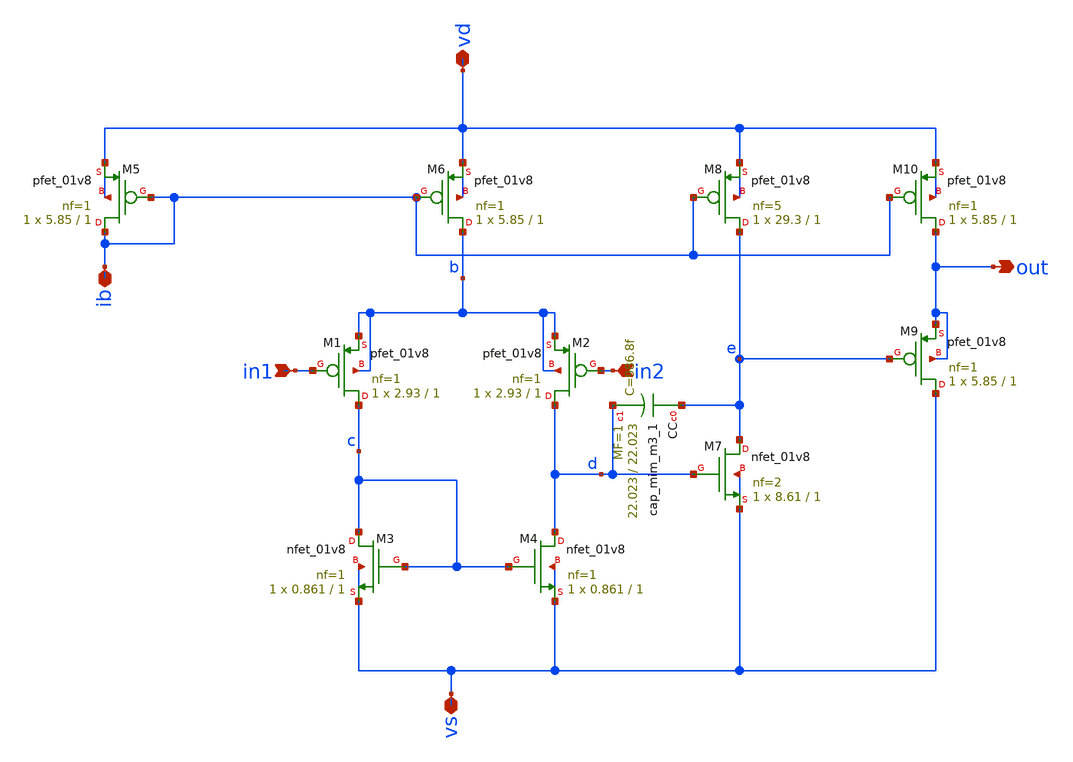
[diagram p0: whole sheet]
** sch_path: xschem/ota.sch
* Copyright 2020 Stefan Frederik Schippers
* Licensed under the Apache License, Version 2.0 (the "License");
* you may not use this file except in compliance with the License.
* You may obtain a copy of the License at
* https://www.apache.org/licenses/LICENSE-2.0
* Unless required by applicable law or agreed to in writing, software
* distributed under the License is distributed on an "AS IS" BASIS,
* WITHOUT WARRANTIES OR CONDITIONS OF ANY KIND, either express or implied.
* See the License for the specific language governing permissions and
* limitations under the License.
**.subckt ota vd vs ib in1 in2 out
*.iopin vd
*.iopin vs
*.iopin ib
*.ipin in1
*.ipin in2
*.opin out
XM4 d c vs vs sky130_fd_pr__nfet_01v8 L=1 W=0.861 nf=1 ad='int((nf+1)/2) * W/nf * 0.29' as='int((nf+2)/2) * W/nf * 0.29'
+ pd='2*int((nf+1)/2) * (W/nf + 0.29)' ps='2*int((nf+2)/2) * (W/nf + 0.29)' nrd='0.29 / W' nrs='0.29 / W'
+ sa=0 sb=0 sd=0 mult=1 m=1
XM7 e d vs vs sky130_fd_pr__nfet_01v8 L=1 W=8.61 nf=2 ad='int((nf+1)/2) * W/nf * 0.29' as='int((nf+2)/2) * W/nf * 0.29'
+ pd='2*int((nf+1)/2) * (W/nf + 0.29)' ps='2*int((nf+2)/2) * (W/nf + 0.29)' nrd='0.29 / W' nrs='0.29 / W'
+ sa=0 sb=0 sd=0 mult=1 m=1
XM5 ib ib vd vd sky130_fd_pr__pfet_01v8 L=1 W=5.85 nf=1 ad='int((nf+1)/2) * W/nf * 0.29' as='int((nf+2)/2) * W/nf * 0.29'
+ pd='2*int((nf+1)/2) * (W/nf + 0.29)' ps='2*int((nf+2)/2) * (W/nf + 0.29)' nrd='0.29 / W' nrs='0.29 / W'
+ sa=0 sb=0 sd=0 mult=1 m=1
XM6 b ib vd vd sky130_fd_pr__pfet_01v8 L=1 W=5.85 nf=1 ad='int((nf+1)/2) * W/nf * 0.29' as='int((nf+2)/2) * W/nf * 0.29'
+ pd='2*int((nf+1)/2) * (W/nf + 0.29)' ps='2*int((nf+2)/2) * (W/nf + 0.29)' nrd='0.29 / W' nrs='0.29 / W'
+ sa=0 sb=0 sd=0 mult=1 m=1
XM8 e ib vd vd sky130_fd_pr__pfet_01v8 L=1 W=29.3 nf=5 ad='int((nf+1)/2) * W/nf * 0.29' as='int((nf+2)/2) * W/nf * 0.29'
+ pd='2*int((nf+1)/2) * (W/nf + 0.29)' ps='2*int((nf+2)/2) * (W/nf + 0.29)' nrd='0.29 / W' nrs='0.29 / W'
+ sa=0 sb=0 sd=0 mult=1 m=1
XM10 out ib vd vd sky130_fd_pr__pfet_01v8 L=1 W=5.85 nf=1 ad='int((nf+1)/2) * W/nf * 0.29' as='int((nf+2)/2) * W/nf * 0.29'
+ pd='2*int((nf+1)/2) * (W/nf + 0.29)' ps='2*int((nf+2)/2) * (W/nf + 0.29)' nrd='0.29 / W' nrs='0.29 / W'
+ sa=0 sb=0 sd=0 mult=1 m=1
XM9 vs e out out sky130_fd_pr__pfet_01v8 L=1 W=5.85 nf=1 ad='int((nf+1)/2) * W/nf * 0.29' as='int((nf+2)/2) * W/nf * 0.29'
+ pd='2*int((nf+1)/2) * (W/nf + 0.29)' ps='2*int((nf+2)/2) * (W/nf + 0.29)' nrd='0.29 / W' nrs='0.29 / W'
+ sa=0 sb=0 sd=0 mult=1 m=1
XM1 c in1 b b sky130_fd_pr__pfet_01v8 L=1 W=2.93 nf=1 ad='int((nf+1)/2) * W/nf * 0.29' as='int((nf+2)/2) * W/nf * 0.29'
+ pd='2*int((nf+1)/2) * (W/nf + 0.29)' ps='2*int((nf+2)/2) * (W/nf + 0.29)' nrd='0.29 / W' nrs='0.29 / W'
+ sa=0 sb=0 sd=0 mult=1 m=1
XM2 d in2 b b sky130_fd_pr__pfet_01v8 L=1 W=2.93 nf=1 ad='int((nf+1)/2) * W/nf * 0.29' as='int((nf+2)/2) * W/nf * 0.29'
+ pd='2*int((nf+1)/2) * (W/nf + 0.29)' ps='2*int((nf+2)/2) * (W/nf + 0.29)' nrd='0.29 / W' nrs='0.29 / W'
+ sa=0 sb=0 sd=0 mult=1 m=1
XM3 c c vs vs sky130_fd_pr__nfet_01v8 L=1 W=0.861 nf=1 ad='int((nf+1)/2) * W/nf * 0.29' as='int((nf+2)/2) * W/nf * 0.29'
+ pd='2*int((nf+1)/2) * (W/nf + 0.29)' ps='2*int((nf+2)/2) * (W/nf + 0.29)' nrd='0.29 / W' nrs='0.29 / W'
+ sa=0 sb=0 sd=0 mult=1 m=1
XCC e d sky130_fd_pr__cap_mim_m3_1 W=22.023 L=22.023 MF=1 m=1
**.ends
.end
